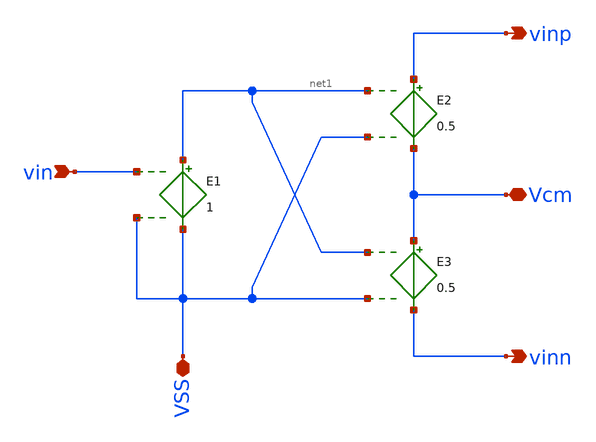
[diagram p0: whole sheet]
** sch_path: sky130/macros/iqmod/schematic/single2dm.sch
**.subckt single2dm vin vinn Vcm vinp VSS
*.ipin vin
*.opin vinn
*.iopin Vcm
*.opin vinp
*.iopin VSS
E3 Vcm vinn net1 VSS 0.5
E2 vinp Vcm net1 VSS 0.5
E1 net1 VSS vin VSS 1
**.ends
.end
